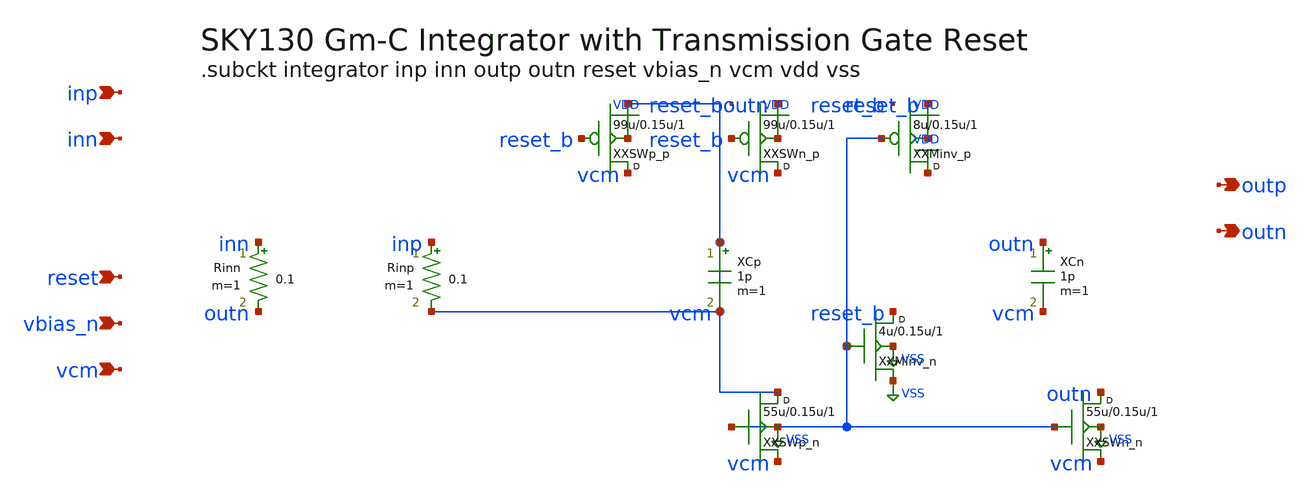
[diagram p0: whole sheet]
** sch_path: data/sch/ode_integrator.sch
**.subckt ode_integrator inp inn outp outn reset vbias_n vcm
*.ipin inp
*.ipin inn
*.opin outp
*.opin outn
*.ipin reset
*.ipin vbias_n
*.ipin vcm
XXMinv_n reset_b VSS VSS VSS sky130_fd_pr__nfet_01v8 w=4u l=0.15u m=1
XXMinv_p VDD VSS reset_b VDD sky130_fd_pr__pfet_01v8 w=8u l=0.15u m=1
XCp vcm vcm 1p m=1
XXSWp_n vcm VSS vcm VSS sky130_fd_pr__nfet_01v8_lvt w=55u l=0.15u m=1
XXSWp_p vcm reset_b vcm VDD sky130_fd_pr__pfet_01v8 w=99u l=0.15u m=1
XCn outn vcm 1p m=1
XXSWn_n outn VSS vcm VSS sky130_fd_pr__nfet_01v8_lvt w=55u l=0.15u m=1
XXSWn_p vcm reset_b outn VDD sky130_fd_pr__pfet_01v8 w=99u l=0.15u m=1
Rinp inp vcm 0.1 m=1
Rinn inn outn 0.1 m=1
**.ends
.GLOBAL VSS
.GLOBAL VDD
.end
